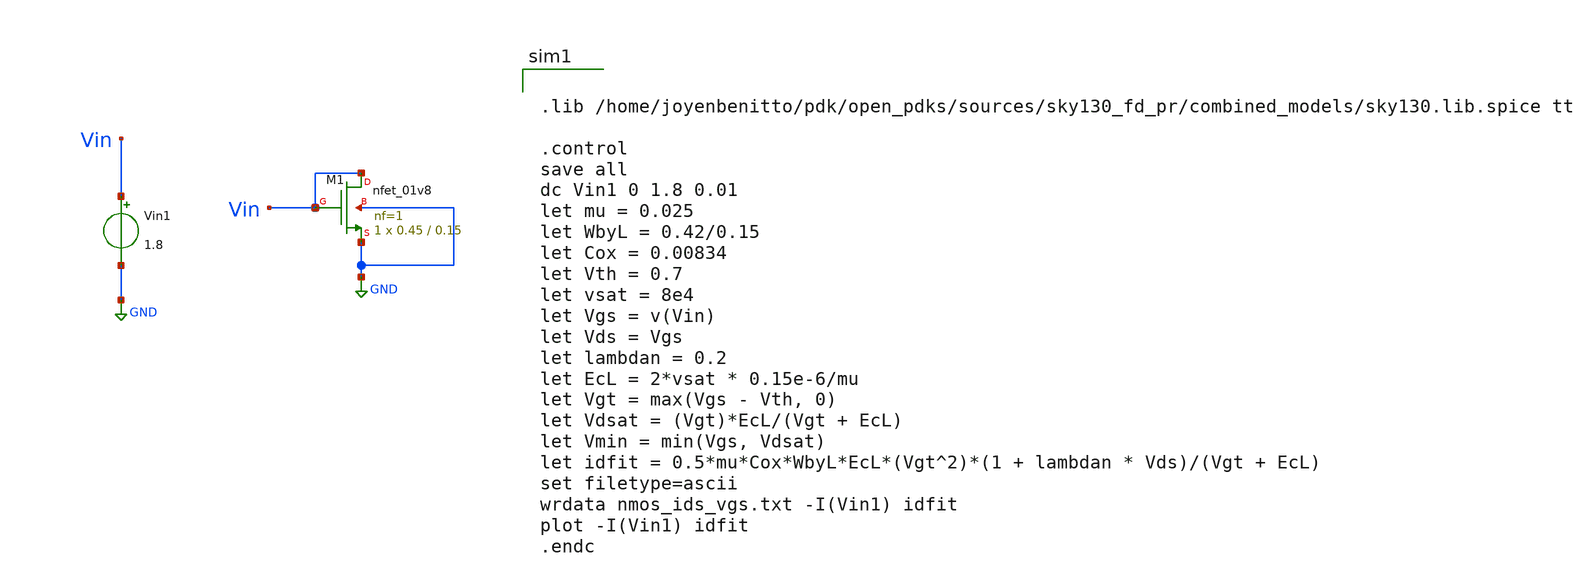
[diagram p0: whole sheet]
** sch_path: tutorials/tutorial_1/tutorial1a.sch
**.subckt tutorial1a
XM1 Vin Vin GND GND sky130_fd_pr__nfet_01v8 L=0.15 W=0.45 nf=1 ad='int((1 + 1)/2) * 0.45 / 1 * 0.29'
+ as='int((1 + 2)/2) * 0.45 / 1 * 0.29' pd='2*int((1 + 1)/2) * (0.45 / 1 + 0.29)' ps='2*int((1 + 2)/2) * (0.45 / 1 + 0.29)'
+ nrd='0.29 / 0.45 ' nrs='0.29 / 0.45 ' sa=0 sb=0 sd=0 mult=1 m=1
Vin1 Vin GND 1.8
**** begin user architecture code


.lib /home/joyenbenitto/pdk/open_pdks/sources/sky130_fd_pr/combined_models/sky130.lib.spice tt

.control
save all
dc Vin1 0 1.8 0.01
let mu = 0.025
let WbyL = 0.42/0.15
let Cox = 0.00834
let Vth = 0.7
let vsat = 8e4
let Vgs = v(Vin)
let Vds = Vgs
let lambdan = 0.2
let EcL = 2*vsat * 0.15e-6/mu
let Vgt = max(Vgs - Vth, 0)
let Vdsat = (Vgt)*EcL/(Vgt + EcL)
let Vmin = min(Vgs, Vdsat)
let idfit = 0.5*mu*Cox*WbyL*EcL*(Vgt^2)*(1 + lambdan * Vds)/(Vgt + EcL)
set filetype=ascii
wrdata nmos_ids_vgs.txt -I(Vin1) idfit
plot -I(Vin1) idfit
.endc


**** end user architecture code
**.ends
.GLOBAL GND
.end
